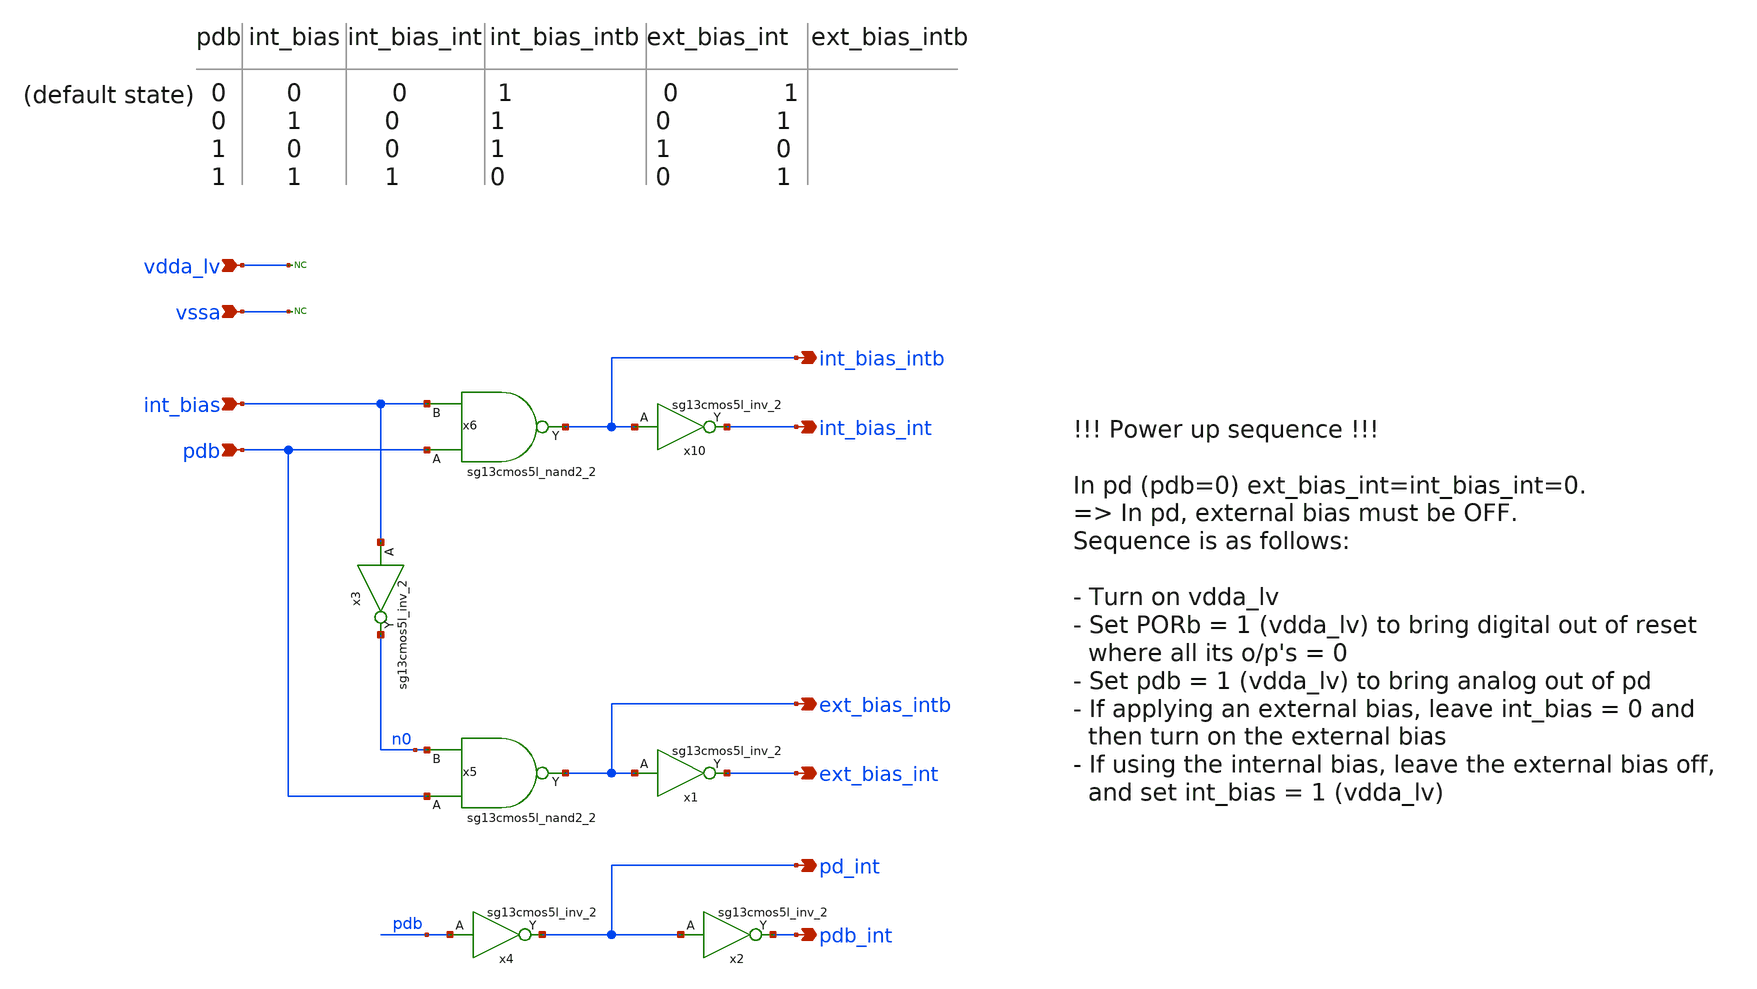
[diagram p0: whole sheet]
** sch_path: Schematics_Layout/sunrise_logic_pd_bias/sunrise_logic_pd_bias.sch
**.subckt sunrise_logic_pd_bias vdda_lv vssa int_bias pdb int_bias_int int_bias_intb ext_bias_int
*+ ext_bias_intb pd_int pdb_int
*.ipin vdda_lv
*.ipin vssa
*.ipin int_bias
*.ipin pdb
*.opin int_bias_int
*.opin int_bias_intb
*.opin ext_bias_int
*.opin ext_bias_intb
*.opin pd_int
*.opin pdb_int
* noconn vdda_lv
* noconn vssa
x10 int_bias_int int_bias_intb vdda_lv vssa sg13cmos5l_inv_2
x1 ext_bias_int ext_bias_intb vdda_lv vssa sg13cmos5l_inv_2
x2 pdb_int pd_int vdda_lv vssa sg13cmos5l_inv_2
x4 pd_int pdb vdda_lv vssa sg13cmos5l_inv_2
x3 n0 int_bias vdda_lv vssa sg13cmos5l_inv_2
x5 ext_bias_intb pdb n0 vdda_lv vssa sg13cmos5l_nand2_2
x6 int_bias_intb pdb int_bias vdda_lv vssa sg13cmos5l_nand2_2
**.ends
.end
